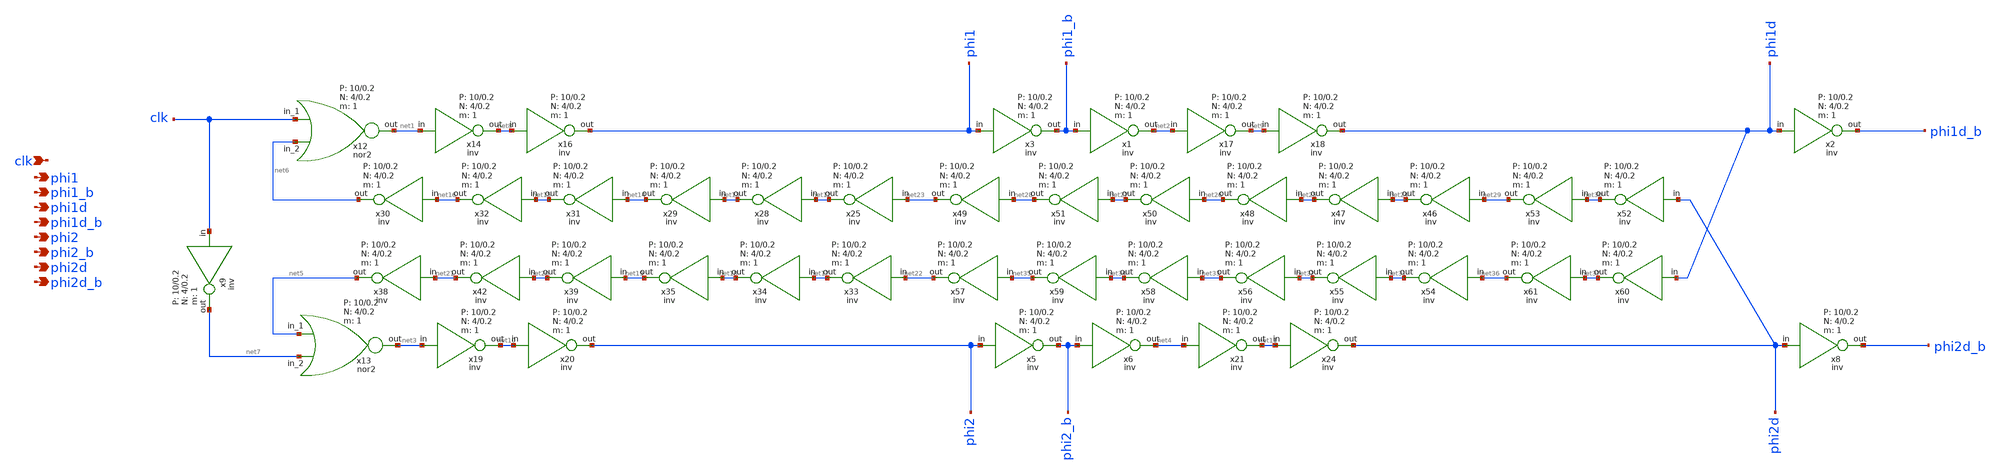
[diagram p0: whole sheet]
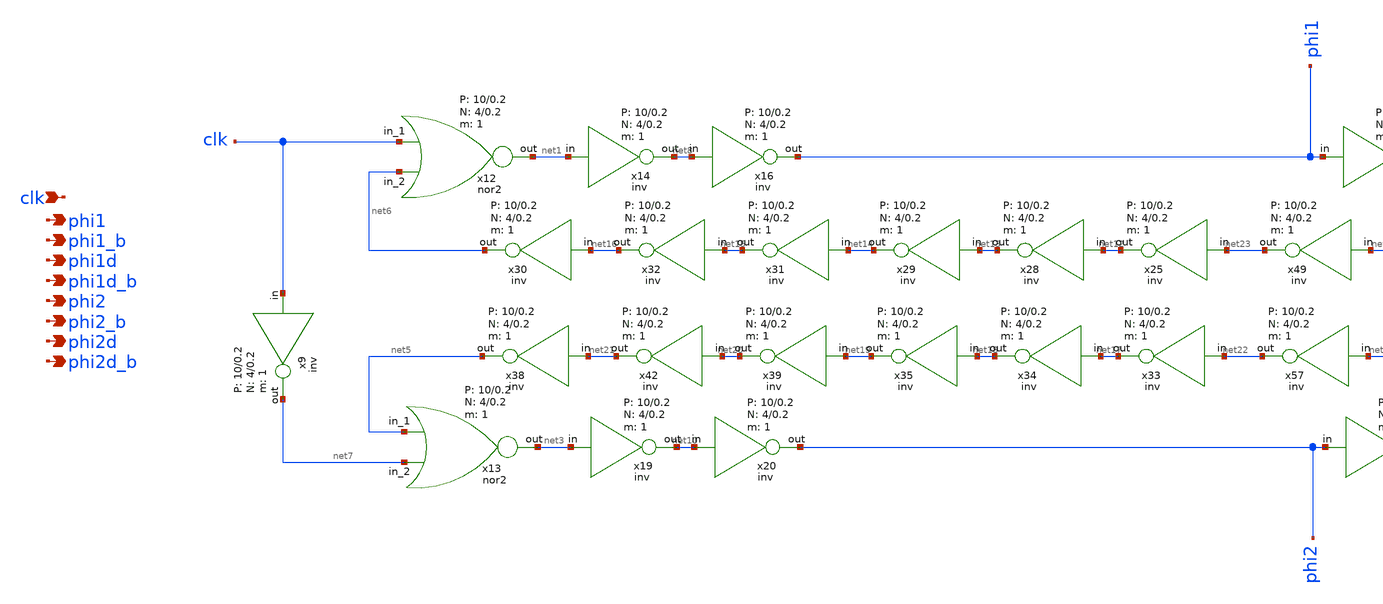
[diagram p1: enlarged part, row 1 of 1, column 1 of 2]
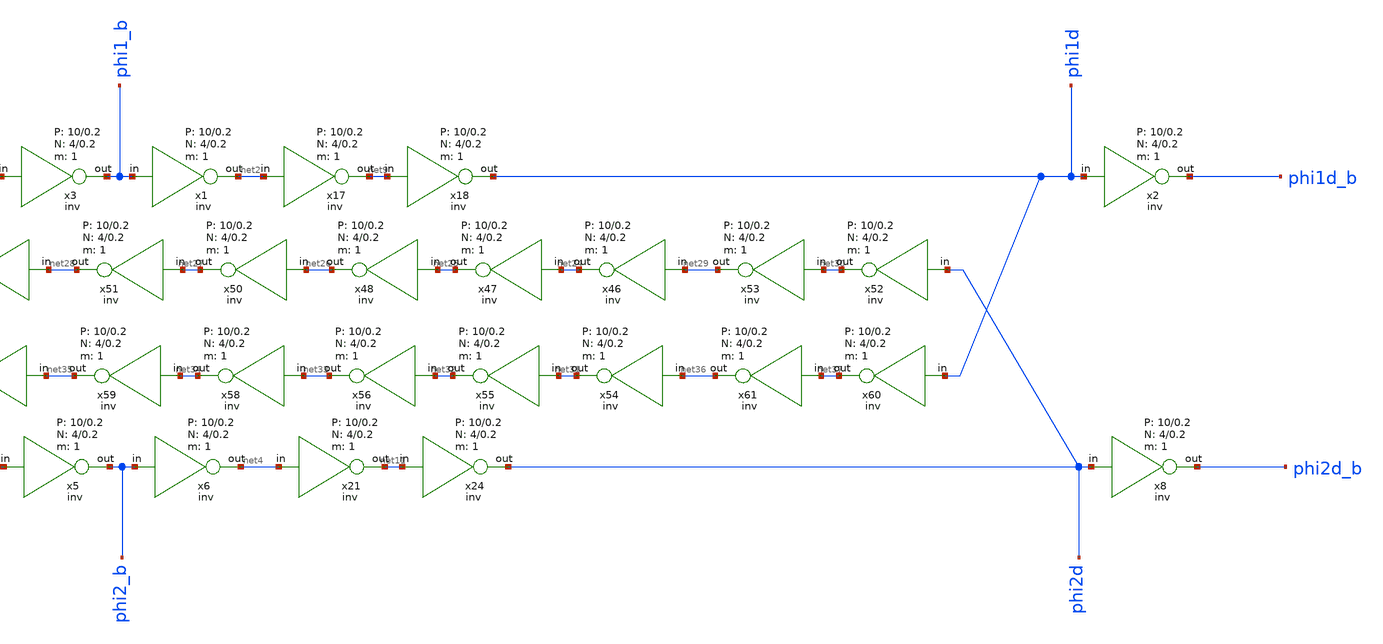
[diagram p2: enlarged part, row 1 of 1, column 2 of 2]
** sch_path: design/schematic/clock_custom_cell.sch
**.subckt clock_custom_cell phi1 phi1_b phi1d phi1d_b phi2 phi2_b phi2d phi2d_b clk
*.opin phi1
*.opin phi1_b
*.opin phi1d
*.opin phi1d_b
*.opin phi2
*.opin phi2_b
*.opin phi2d
*.opin phi2d_b
*.ipin clk
x3 phi1 phi1_b VDD GND 1 4 0.2 10 0.2 inv
x1 phi1_b net2 VDD GND 1 4 0.2 10 0.2 inv
x2 phi1d phi1d_b VDD GND 1 4 0.2 10 0.2 inv
x5 phi2 phi2_b VDD GND 1 4 0.2 10 0.2 inv
x6 phi2_b net4 VDD GND 1 4 0.2 10 0.2 inv
x8 phi2d phi2d_b VDD GND 1 4 0.2 10 0.2 inv
x9 clk net7 VDD GND 1 4 0.2 10 0.2 inv
x12 clk net6 net1 VDD GND 1 4 0.2 10 0.2 nor2
x13 net5 net7 net3 VDD GND 1 4 0.2 10 0.2 nor2
x14 net1 net8 VDD GND 1 4 0.2 10 0.2 inv
x16 net8 phi1 VDD GND 1 4 0.2 10 0.2 inv
x17 net2 net9 VDD GND 1 4 0.2 10 0.2 inv
x18 net9 phi1d VDD GND 1 4 0.2 10 0.2 inv
x19 net3 net10 VDD GND 1 4 0.2 10 0.2 inv
x20 net10 phi2 VDD GND 1 4 0.2 10 0.2 inv
x21 net4 net11 VDD GND 1 4 0.2 10 0.2 inv
x24 net11 phi2d VDD GND 1 4 0.2 10 0.2 inv
x25 net23 net12 VDD GND 1 4 0.2 10 0.2 inv
x28 net12 net13 VDD GND 1 4 0.2 10 0.2 inv
x29 net13 net14 VDD GND 1 4 0.2 10 0.2 inv
x30 net16 net6 VDD GND 1 4 0.2 10 0.2 inv
x31 net14 net15 VDD GND 1 4 0.2 10 0.2 inv
x32 net15 net16 VDD GND 1 4 0.2 10 0.2 inv
x33 net22 net17 VDD GND 1 4 0.2 10 0.2 inv
x34 net17 net18 VDD GND 1 4 0.2 10 0.2 inv
x35 net18 net19 VDD GND 1 4 0.2 10 0.2 inv
x38 net21 net5 VDD GND 1 4 0.2 10 0.2 inv
x39 net19 net20 VDD GND 1 4 0.2 10 0.2 inv
x42 net20 net21 VDD GND 1 4 0.2 10 0.2 inv
x46 net29 net24 VDD GND 1 4 0.2 10 0.2 inv
x47 net24 net25 VDD GND 1 4 0.2 10 0.2 inv
x48 net25 net26 VDD GND 1 4 0.2 10 0.2 inv
x49 net28 net23 VDD GND 1 4 0.2 10 0.2 inv
x50 net26 net27 VDD GND 1 4 0.2 10 0.2 inv
x51 net27 net28 VDD GND 1 4 0.2 10 0.2 inv
x52 phi2d net30 VDD GND 1 4 0.2 10 0.2 inv
x53 net30 net29 VDD GND 1 4 0.2 10 0.2 inv
x54 net36 net31 VDD GND 1 4 0.2 10 0.2 inv
x55 net31 net32 VDD GND 1 4 0.2 10 0.2 inv
x56 net32 net33 VDD GND 1 4 0.2 10 0.2 inv
x57 net35 net22 VDD GND 1 4 0.2 10 0.2 inv
x58 net33 net34 VDD GND 1 4 0.2 10 0.2 inv
x59 net34 net35 VDD GND 1 4 0.2 10 0.2 inv
x60 phi1d net37 VDD GND 1 4 0.2 10 0.2 inv
x61 net37 net36 VDD GND 1 4 0.2 10 0.2 inv
**.ends

* expanding   symbol:  inv.sym # of pins=2
** sym_path: design/schematic/inv.sym
** sch_path: design/schematic/inv.sch
.subckt inv in out VDD VSS N W_N L_N W_P L_P    N=1 W_N=2 L_N=0.2 W_P=5 L_P=0.2
*.ipin in
*.opin out
XM2 out in VSS VSS sky130_fd_pr__nfet_01v8 L=L_N W=W_N nf=1 ad='int((nf+1)/2) * W/nf * 0.29' as='int((nf+2)/2) * W/nf * 0.29'
+ pd='2*int((nf+1)/2) * (W/nf + 0.29)' ps='2*int((nf+2)/2) * (W/nf + 0.29)' nrd='0.29 / W' nrs='0.29 / W'
+ sa=0 sb=0 sd=0 mult=N m=N
XM1 out in VDD VDD sky130_fd_pr__pfet_01v8 L=L_P W=W_P nf=1 ad='int((nf+1)/2) * W/nf * 0.29' as='int((nf+2)/2) * W/nf * 0.29'
+ pd='2*int((nf+1)/2) * (W/nf + 0.29)' ps='2*int((nf+2)/2) * (W/nf + 0.29)' nrd='0.29 / W' nrs='0.29 / W'
+ sa=0 sb=0 sd=0 mult=N m=N
.ends


* expanding   symbol:  nor2.sym # of pins=3
** sym_path: design/schematic/nor2.sym
** sch_path: design/schematic/nor2.sch
.subckt nor2 in_1 in_2 out VDD VSS N W_N L_N W_P L_P    N=1 W_N=4 L_N=0.15 W_P=10 L_P=0.15
*.ipin in_1
*.ipin in_2
*.opin out
XM1 out in_2 VSS VSS sky130_fd_pr__nfet_01v8 L=L_N W=W_N nf=1 ad='int((nf+1)/2) * W/nf * 0.29' as='int((nf+2)/2) * W/nf * 0.29'
+ pd='2*int((nf+1)/2) * (W/nf + 0.29)' ps='2*int((nf+2)/2) * (W/nf + 0.29)' nrd='0.29 / W' nrs='0.29 / W'
+ sa=0 sb=0 sd=0 mult=N m=N
XM2 out in_1 VSS VSS sky130_fd_pr__nfet_01v8 L=L_N W=W_N nf=1 ad='int((nf+1)/2) * W/nf * 0.29' as='int((nf+2)/2) * W/nf * 0.29'
+ pd='2*int((nf+1)/2) * (W/nf + 0.29)' ps='2*int((nf+2)/2) * (W/nf + 0.29)' nrd='0.29 / W' nrs='0.29 / W'
+ sa=0 sb=0 sd=0 mult=N m=N
XM3 out in_2 net1 VDD sky130_fd_pr__pfet_01v8 L=L_P W=W_P nf=1 ad='int((nf+1)/2) * W/nf * 0.29' as='int((nf+2)/2) * W/nf * 0.29'
+ pd='2*int((nf+1)/2) * (W/nf + 0.29)' ps='2*int((nf+2)/2) * (W/nf + 0.29)' nrd='0.29 / W' nrs='0.29 / W'
+ sa=0 sb=0 sd=0 mult=N m=N
XM4 net1 in_1 VDD VDD sky130_fd_pr__pfet_01v8 L=L_P W=W_P nf=1 ad='int((nf+1)/2) * W/nf * 0.29' as='int((nf+2)/2) * W/nf * 0.29'
+ pd='2*int((nf+1)/2) * (W/nf + 0.29)' ps='2*int((nf+2)/2) * (W/nf + 0.29)' nrd='0.29 / W' nrs='0.29 / W'
+ sa=0 sb=0 sd=0 mult=N m=N
.ends

.end
